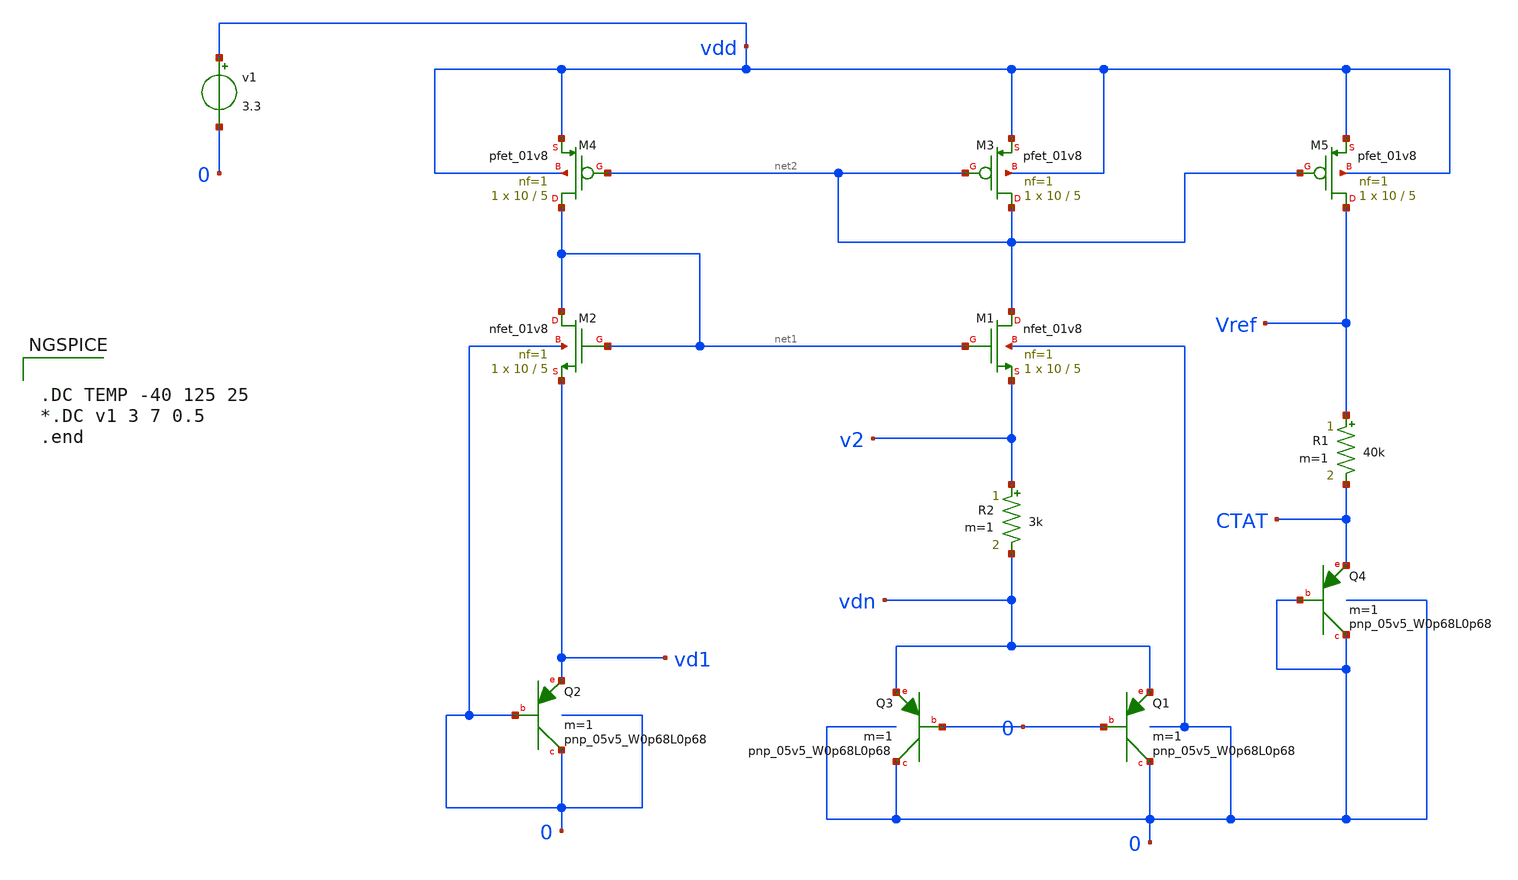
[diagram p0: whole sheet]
** sch_path: Bandgap/PTAT_CTAT.sch
**.subckt PTAT_CTAT
v1 vdd 0 3.3
XQ2 0 0 vd1 sky130_fd_pr__pnp_05v5_W0p68L0p68 m=1
XQ1 0 0 vdn sky130_fd_pr__pnp_05v5_W0p68L0p68 m=1
XQ3 0 0 vdn sky130_fd_pr__pnp_05v5_W0p68L0p68 m=1
XM1 net2 net1 v2 0 sky130_fd_pr__nfet_01v8 L=5 W=10 nf=1 ad='int((nf+1)/2) * W/nf * 0.29' as='int((nf+2)/2) * W/nf * 0.29'
+ pd='2*int((nf+1)/2) * (W/nf + 0.29)' ps='2*int((nf+2)/2) * (W/nf + 0.29)' nrd='0.29 / W' nrs='0.29 / W'
+ sa=0 sb=0 sd=0 mult=1 m=1
XM2 net1 net1 vd1 0 sky130_fd_pr__nfet_01v8 L=5 W=10 nf=1 ad='int((nf+1)/2) * W/nf * 0.29' as='int((nf+2)/2) * W/nf * 0.29'
+ pd='2*int((nf+1)/2) * (W/nf + 0.29)' ps='2*int((nf+2)/2) * (W/nf + 0.29)' nrd='0.29 / W' nrs='0.29 / W'
+ sa=0 sb=0 sd=0 mult=1 m=1
XM3 net2 net2 vdd vdd sky130_fd_pr__pfet_01v8 L=5 W=10 nf=1 ad='int((nf+1)/2) * W/nf * 0.29' as='int((nf+2)/2) * W/nf * 0.29'
+ pd='2*int((nf+1)/2) * (W/nf + 0.29)' ps='2*int((nf+2)/2) * (W/nf + 0.29)' nrd='0.29 / W' nrs='0.29 / W'
+ sa=0 sb=0 sd=0 mult=1 m=1
XM4 net1 net2 vdd vdd sky130_fd_pr__pfet_01v8 L=5 W=10 nf=1 ad='int((nf+1)/2) * W/nf * 0.29' as='int((nf+2)/2) * W/nf * 0.29'
+ pd='2*int((nf+1)/2) * (W/nf + 0.29)' ps='2*int((nf+2)/2) * (W/nf + 0.29)' nrd='0.29 / W' nrs='0.29 / W'
+ sa=0 sb=0 sd=0 mult=1 m=1
XM5 Vref net2 vdd vdd sky130_fd_pr__pfet_01v8 L=5 W=10 nf=1 ad='int((nf+1)/2) * W/nf * 0.29' as='int((nf+2)/2) * W/nf * 0.29'
+ pd='2*int((nf+1)/2) * (W/nf + 0.29)' ps='2*int((nf+2)/2) * (W/nf + 0.29)' nrd='0.29 / W' nrs='0.29 / W'
+ sa=0 sb=0 sd=0 mult=1 m=1
XQ4 0 0 CTAT sky130_fd_pr__pnp_05v5_W0p68L0p68 m=1
R1 Vref CTAT 40k m=1
R2 v2 vdn 3k m=1
**** begin user architecture code

.include $::SKYWATER_MODELS/cells/nfet_01v8/sky130_fd_pr__nfet_01v8__tt.corner.spice
.include $::SKYWATER_MODELS/cells/nfet_01v8_lvt/sky130_fd_pr__nfet_01v8_lvt__tt.corner.spice
.include $::SKYWATER_MODELS/cells/pfet_01v8/sky130_fd_pr__pfet_01v8__tt.corner.spice
.include $::SKYWATER_MODELS/cells/nfet_03v3_nvt/sky130_fd_pr__nfet_03v3_nvt__tt.corner.spice
.include $::SKYWATER_MODELS/cells/nfet_05v0_nvt/sky130_fd_pr__nfet_05v0_nvt__tt.corner.spice
.include $::SKYWATER_MODELS/cells/esd_nfet_01v8/sky130_fd_pr__esd_nfet_01v8__tt.corner.spice
.include $::SKYWATER_MODELS/cells/pfet_01v8_lvt/sky130_fd_pr__pfet_01v8_lvt__tt.corner.spice
.include $::SKYWATER_MODELS/cells/pfet_01v8_hvt/sky130_fd_pr__pfet_01v8_hvt__tt.corner.spice
.include $::SKYWATER_MODELS/cells/esd_pfet_g5v0d10v5/sky130_fd_pr__esd_pfet_g5v0d10v5__tt.corner.spice
.include $::SKYWATER_MODELS/cells/pfet_g5v0d10v5/sky130_fd_pr__pfet_g5v0d10v5__tt.corner.spice
.include $::SKYWATER_MODELS/cells/pfet_g5v0d16v0/sky130_fd_pr__pfet_g5v0d16v0__tt.corner.spice
.include $::SKYWATER_MODELS/cells/nfet_g5v0d10v5/sky130_fd_pr__nfet_g5v0d10v5__tt.corner.spice
.include $::SKYWATER_MODELS/cells/nfet_g5v0d16v0/sky130_fd_pr__nfet_g5v0d16v0__tt_discrete.corner.spice
.include $::SKYWATER_MODELS/cells/esd_nfet_g5v0d10v5/sky130_fd_pr__esd_nfet_g5v0d10v5__tt.corner.spice
.include $::SKYWATER_MODELS/models/corners/tt/nonfet.spice
* Mismatch parameters
.include $::SKYWATER_MODELS/cells/nfet_01v8/sky130_fd_pr__nfet_01v8__mismatch.corner.spice
.include $::SKYWATER_MODELS/cells/pfet_01v8/sky130_fd_pr__pfet_01v8__mismatch.corner.spice
.include $::SKYWATER_MODELS/cells/nfet_01v8_lvt/sky130_fd_pr__nfet_01v8_lvt__mismatch.corner.spice
.include $::SKYWATER_MODELS/cells/pfet_01v8_lvt/sky130_fd_pr__pfet_01v8_lvt__mismatch.corner.spice
.include $::SKYWATER_MODELS/cells/pfet_01v8_hvt/sky130_fd_pr__pfet_01v8_hvt__mismatch.corner.spice
.include $::SKYWATER_MODELS/cells/nfet_g5v0d10v5/sky130_fd_pr__nfet_g5v0d10v5__mismatch.corner.spice
.include $::SKYWATER_MODELS/cells/pfet_g5v0d10v5/sky130_fd_pr__pfet_g5v0d10v5__mismatch.corner.spice
.include $::SKYWATER_MODELS/cells/nfet_05v0_nvt/sky130_fd_pr__nfet_05v0_nvt__mismatch.corner.spice
.include $::SKYWATER_MODELS/cells/nfet_03v3_nvt/sky130_fd_pr__nfet_03v3_nvt__mismatch.corner.spice
* Resistor$::SKYWATER_MODELS/Capacitor
.include $::SKYWATER_MODELS/models/r+c/res_typical__cap_typical.spice
.include $::SKYWATER_MODELS/models/r+c/res_typical__cap_typical__lin.spice
* Special cells
.include $::SKYWATER_MODELS/models/corners/tt/specialized_cells.spice
* All models
.include $::SKYWATER_MODELS/models/all.spice
* Corner
.include $::SKYWATER_MODELS/models/corners/tt/rf.spice



.DC TEMP -40 125 25
*.DC v1 3 7 0.5
.end


**** end user architecture code
**.ends
.end
